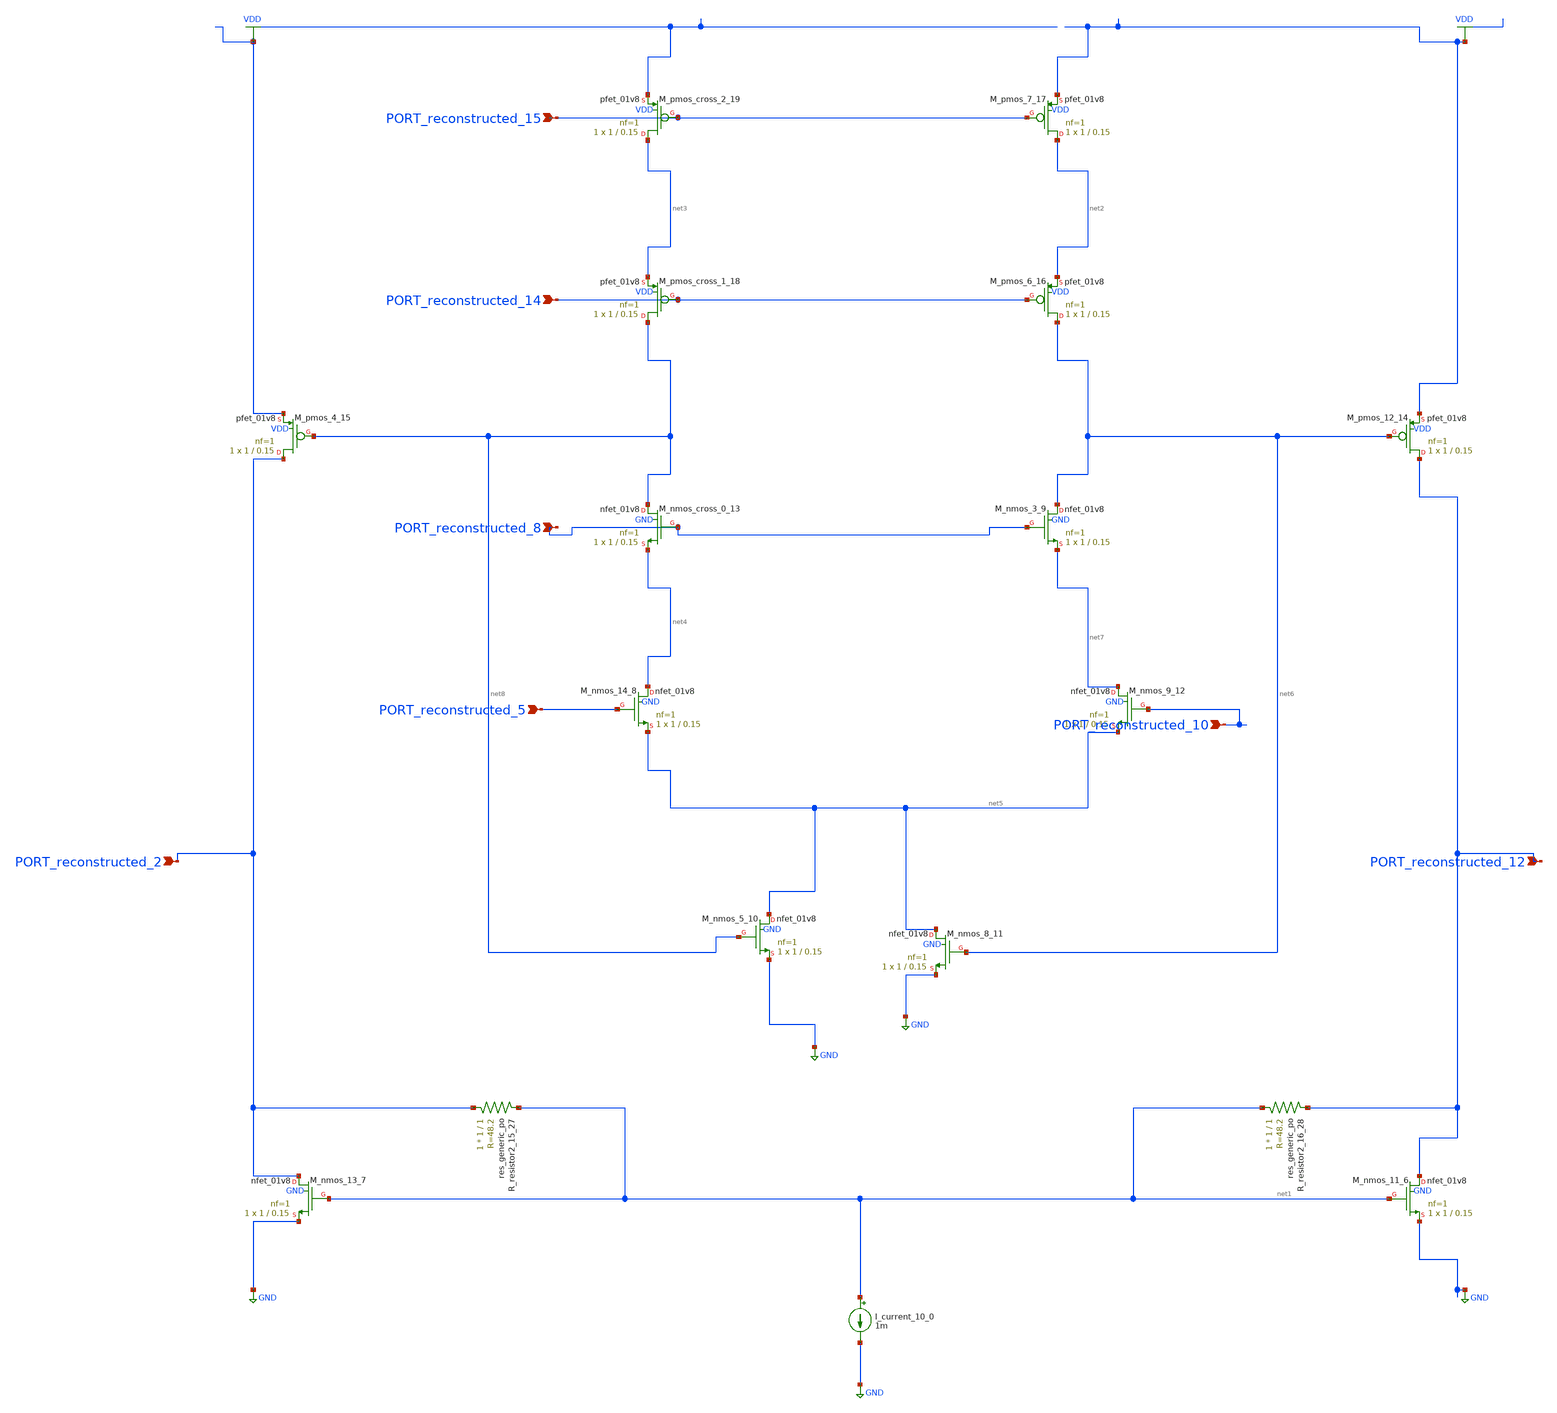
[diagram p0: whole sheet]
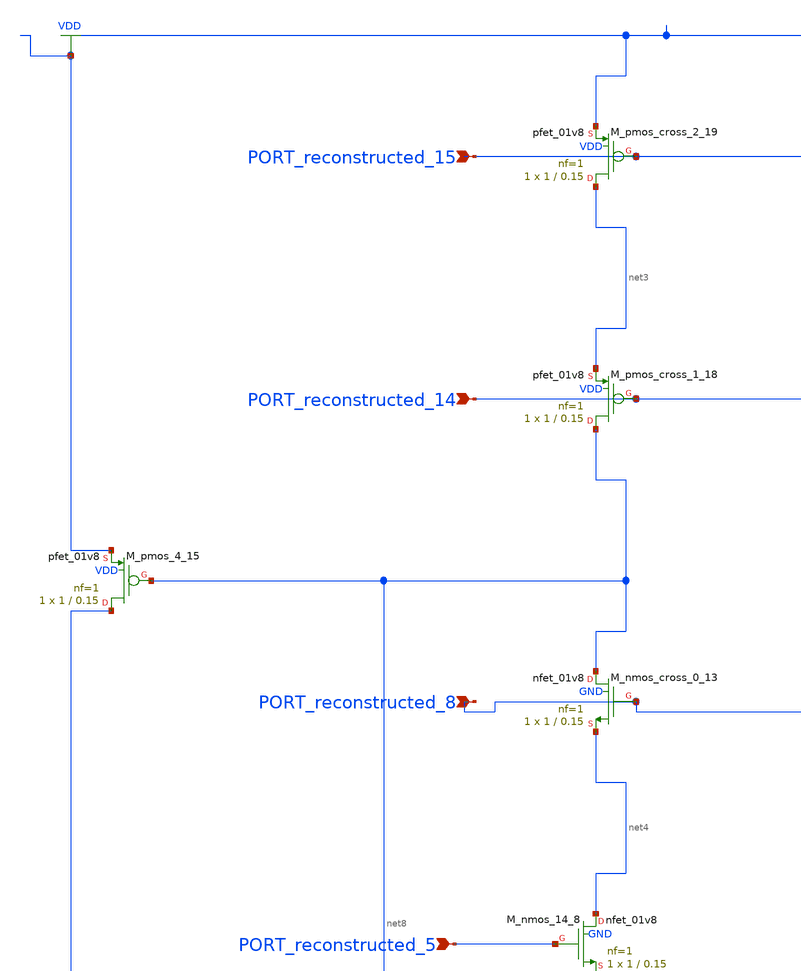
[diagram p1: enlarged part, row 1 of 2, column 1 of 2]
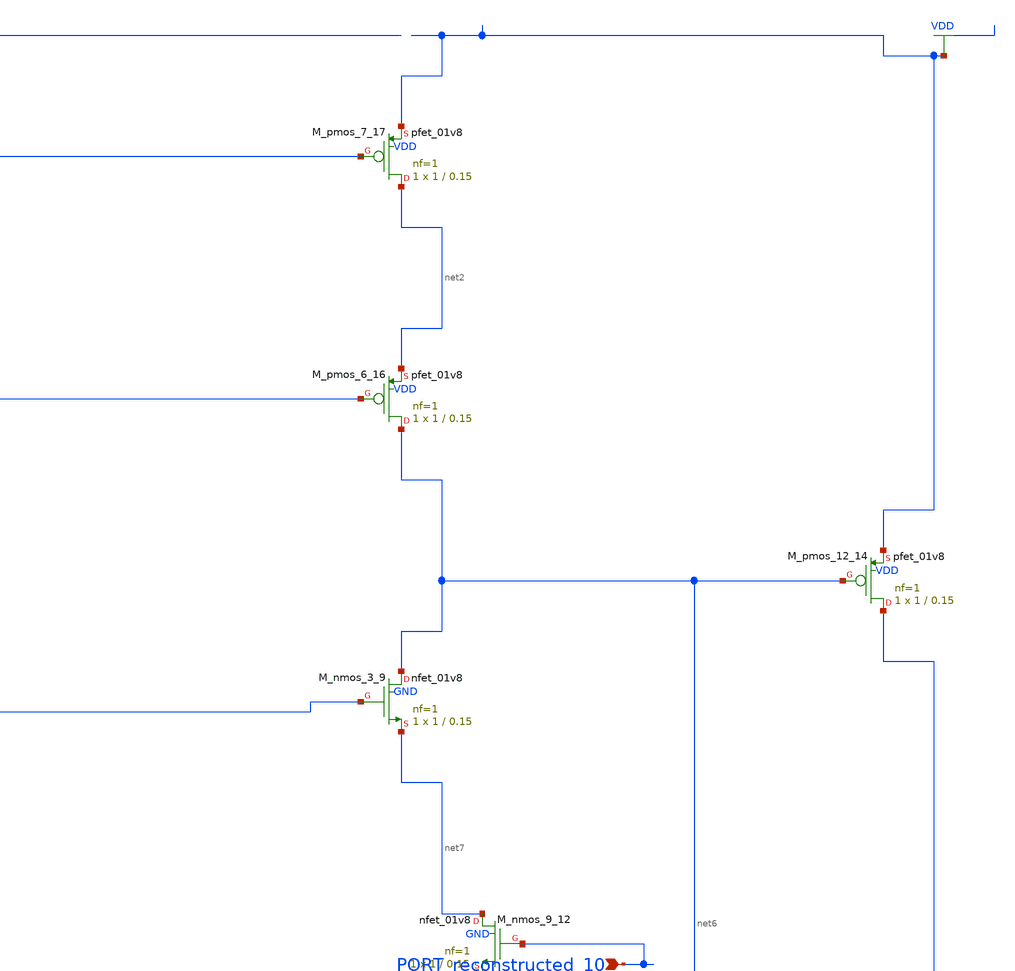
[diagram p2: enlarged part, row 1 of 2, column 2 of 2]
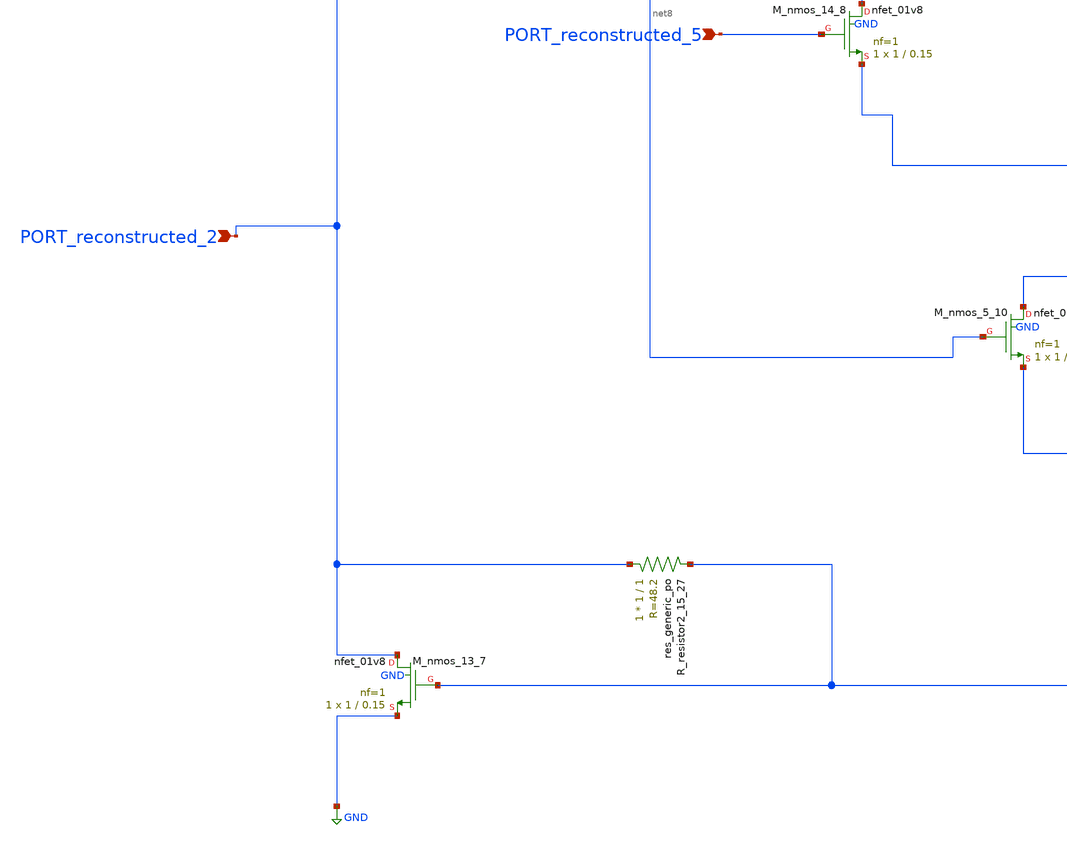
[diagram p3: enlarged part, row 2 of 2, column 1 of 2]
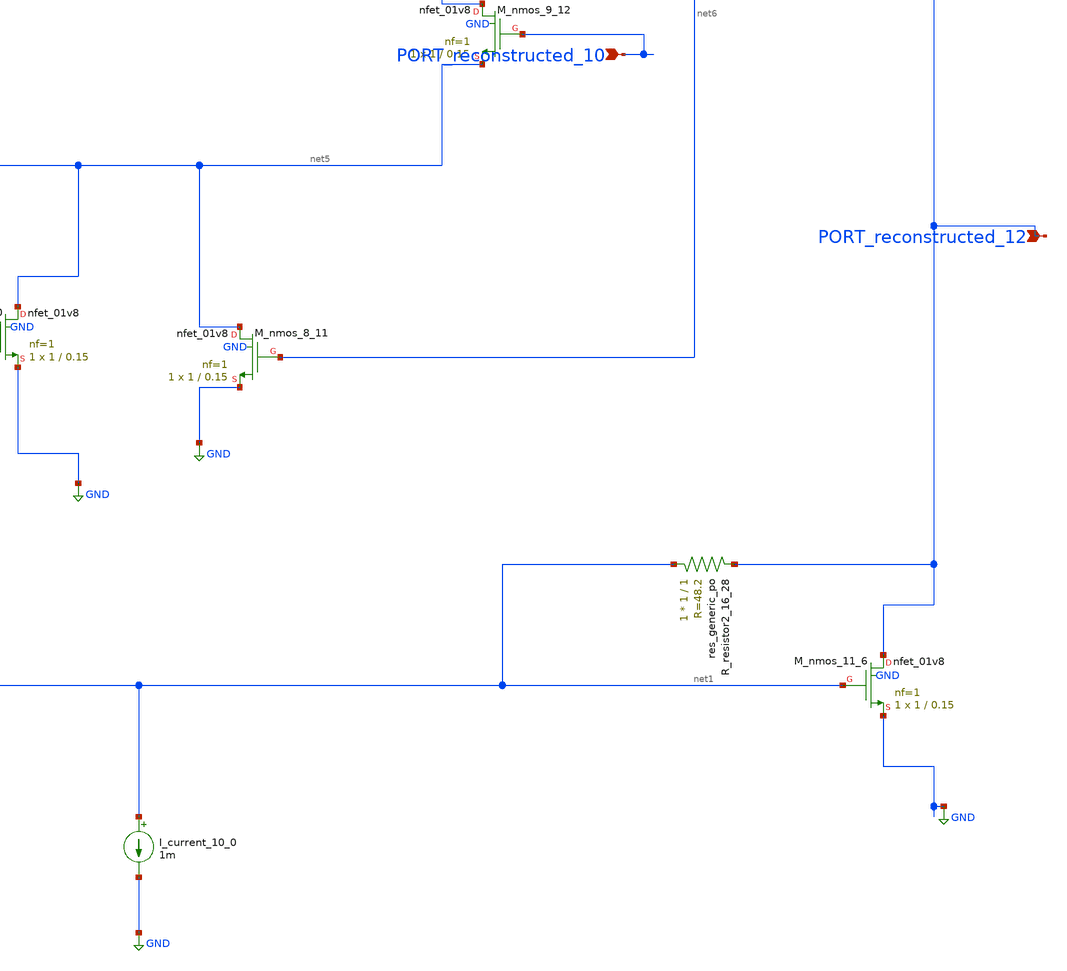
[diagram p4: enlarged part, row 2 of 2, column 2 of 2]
** sch_path: schematics/AMSNet/682.sch
**.subckt 682 PORT_reconstructed_12 PORT_reconstructed_14 PORT_reconstructed_2 PORT_reconstructed_8
*+ PORT_reconstructed_15 PORT_reconstructed_10 PORT_reconstructed_5
*.ipin PORT_reconstructed_12
*.ipin PORT_reconstructed_14
*.ipin PORT_reconstructed_2
*.ipin PORT_reconstructed_8
*.ipin PORT_reconstructed_15
*.ipin PORT_reconstructed_10
*.ipin PORT_reconstructed_5
I_current_10_0 net1 GND 1m
XM_nmos_11_6 PORT_reconstructed_12 net1 GND GND sky130_fd_pr__nfet_01v8 L=0.15 W=1 nf=1 ad='int((1 + 1)/2) * 1 / 1 * 0.29'
+ as='int((1 + 2)/2) * 1 / 1 * 0.29' pd='2*int((1 + 1)/2) * (1 / 1 + 0.29)' ps='2*int((1 + 2)/2) * (1 / 1 + 0.29)'
+ nrd='0.29 / 1 ' nrs='0.29 / 1 ' sa=0 sb=0 sd=0 mult=1 m=1
XM_nmos_13_7 PORT_reconstructed_2 net1 GND GND sky130_fd_pr__nfet_01v8 L=0.15 W=1 nf=1 ad='int((1 + 1)/2) * 1 / 1 * 0.29'
+ as='int((1 + 2)/2) * 1 / 1 * 0.29' pd='2*int((1 + 1)/2) * (1 / 1 + 0.29)' ps='2*int((1 + 2)/2) * (1 / 1 + 0.29)'
+ nrd='0.29 / 1 ' nrs='0.29 / 1 ' sa=0 sb=0 sd=0 mult=1 m=1
XM_nmos_14_8 net4 PORT_reconstructed_5 net5 GND sky130_fd_pr__nfet_01v8 L=0.15 W=1 nf=1 ad='int((1 + 1)/2) * 1 / 1 * 0.29'
+ as='int((1 + 2)/2) * 1 / 1 * 0.29' pd='2*int((1 + 1)/2) * (1 / 1 + 0.29)' ps='2*int((1 + 2)/2) * (1 / 1 + 0.29)'
+ nrd='0.29 / 1 ' nrs='0.29 / 1 ' sa=0 sb=0 sd=0 mult=1 m=1
XM_nmos_3_9 net6 PORT_reconstructed_8 net7 GND sky130_fd_pr__nfet_01v8 L=0.15 W=1 nf=1 ad='int((1 + 1)/2) * 1 / 1 * 0.29'
+ as='int((1 + 2)/2) * 1 / 1 * 0.29' pd='2*int((1 + 1)/2) * (1 / 1 + 0.29)' ps='2*int((1 + 2)/2) * (1 / 1 + 0.29)'
+ nrd='0.29 / 1 ' nrs='0.29 / 1 ' sa=0 sb=0 sd=0 mult=1 m=1
XM_nmos_5_10 net5 net8 GND GND sky130_fd_pr__nfet_01v8 L=0.15 W=1 nf=1 ad='int((1 + 1)/2) * 1 / 1 * 0.29'
+ as='int((1 + 2)/2) * 1 / 1 * 0.29' pd='2*int((1 + 1)/2) * (1 / 1 + 0.29)' ps='2*int((1 + 2)/2) * (1 / 1 + 0.29)'
+ nrd='0.29 / 1 ' nrs='0.29 / 1 ' sa=0 sb=0 sd=0 mult=1 m=1
XM_nmos_8_11 net5 net6 GND GND sky130_fd_pr__nfet_01v8 L=0.15 W=1 nf=1 ad='int((1 + 1)/2) * 1 / 1 * 0.29'
+ as='int((1 + 2)/2) * 1 / 1 * 0.29' pd='2*int((1 + 1)/2) * (1 / 1 + 0.29)' ps='2*int((1 + 2)/2) * (1 / 1 + 0.29)'
+ nrd='0.29 / 1 ' nrs='0.29 / 1 ' sa=0 sb=0 sd=0 mult=1 m=1
XM_nmos_9_12 net7 PORT_reconstructed_10 net5 GND sky130_fd_pr__nfet_01v8 L=0.15 W=1 nf=1 ad='int((1 + 1)/2) * 1 / 1 * 0.29'
+ as='int((1 + 2)/2) * 1 / 1 * 0.29' pd='2*int((1 + 1)/2) * (1 / 1 + 0.29)' ps='2*int((1 + 2)/2) * (1 / 1 + 0.29)'
+ nrd='0.29 / 1 ' nrs='0.29 / 1 ' sa=0 sb=0 sd=0 mult=1 m=1
XM_nmos_cross_0_13 net8 PORT_reconstructed_8 net4 GND sky130_fd_pr__nfet_01v8 L=0.15 W=1 nf=1 ad='int((1 + 1)/2) * 1 / 1 * 0.29'
+ as='int((1 + 2)/2) * 1 / 1 * 0.29' pd='2*int((1 + 1)/2) * (1 / 1 + 0.29)' ps='2*int((1 + 2)/2) * (1 / 1 + 0.29)'
+ nrd='0.29 / 1 ' nrs='0.29 / 1 ' sa=0 sb=0 sd=0 mult=1 m=1
XM_pmos_12_14 PORT_reconstructed_12 net6 VDD VDD sky130_fd_pr__pfet_01v8 L=0.15 W=1 nf=1 ad='int((1 + 1)/2) * 1 / 1 * 0.29'
+ as='int((1 + 2)/2) * 1 / 1 * 0.29' pd='2*int((1 + 1)/2) * (1 / 1 + 0.29)' ps='2*int((1 + 2)/2) * (1 / 1 + 0.29)'
+ nrd='0.29 / 1 ' nrs='0.29 / 1 ' sa=0 sb=0 sd=0 mult=1 m=1
XM_pmos_4_15 PORT_reconstructed_2 net8 VDD VDD sky130_fd_pr__pfet_01v8 L=0.15 W=1 nf=1 ad='int((1 + 1)/2) * 1 / 1 * 0.29'
+ as='int((1 + 2)/2) * 1 / 1 * 0.29' pd='2*int((1 + 1)/2) * (1 / 1 + 0.29)' ps='2*int((1 + 2)/2) * (1 / 1 + 0.29)'
+ nrd='0.29 / 1 ' nrs='0.29 / 1 ' sa=0 sb=0 sd=0 mult=1 m=1
XM_pmos_6_16 net6 PORT_reconstructed_14 net2 VDD sky130_fd_pr__pfet_01v8 L=0.15 W=1 nf=1 ad='int((1 + 1)/2) * 1 / 1 * 0.29'
+ as='int((1 + 2)/2) * 1 / 1 * 0.29' pd='2*int((1 + 1)/2) * (1 / 1 + 0.29)' ps='2*int((1 + 2)/2) * (1 / 1 + 0.29)'
+ nrd='0.29 / 1 ' nrs='0.29 / 1 ' sa=0 sb=0 sd=0 mult=1 m=1
XM_pmos_7_17 net2 PORT_reconstructed_15 VDD VDD sky130_fd_pr__pfet_01v8 L=0.15 W=1 nf=1 ad='int((1 + 1)/2) * 1 / 1 * 0.29'
+ as='int((1 + 2)/2) * 1 / 1 * 0.29' pd='2*int((1 + 1)/2) * (1 / 1 + 0.29)' ps='2*int((1 + 2)/2) * (1 / 1 + 0.29)'
+ nrd='0.29 / 1 ' nrs='0.29 / 1 ' sa=0 sb=0 sd=0 mult=1 m=1
XM_pmos_cross_1_18 net8 PORT_reconstructed_14 net3 VDD sky130_fd_pr__pfet_01v8 L=0.15 W=1 nf=1 ad='int((1 + 1)/2) * 1 / 1 * 0.29'
+ as='int((1 + 2)/2) * 1 / 1 * 0.29' pd='2*int((1 + 1)/2) * (1 / 1 + 0.29)' ps='2*int((1 + 2)/2) * (1 / 1 + 0.29)'
+ nrd='0.29 / 1 ' nrs='0.29 / 1 ' sa=0 sb=0 sd=0 mult=1 m=1
XM_pmos_cross_2_19 net3 PORT_reconstructed_15 VDD VDD sky130_fd_pr__pfet_01v8 L=0.15 W=1 nf=1 ad='int((1 + 1)/2) * 1 / 1 * 0.29'
+ as='int((1 + 2)/2) * 1 / 1 * 0.29' pd='2*int((1 + 1)/2) * (1 / 1 + 0.29)' ps='2*int((1 + 2)/2) * (1 / 1 + 0.29)'
+ nrd='0.29 / 1 ' nrs='0.29 / 1 ' sa=0 sb=0 sd=0 mult=1 m=1
XR_resistor2_15_27 PORT_reconstructed_2 net1 sky130_fd_pr__res_generic_po W=1 L=1 m=1
XR_resistor2_16_28 net1 PORT_reconstructed_12 sky130_fd_pr__res_generic_po W=1 L=1 m=1
**.ends
.GLOBAL GND
.GLOBAL VDD
.end
